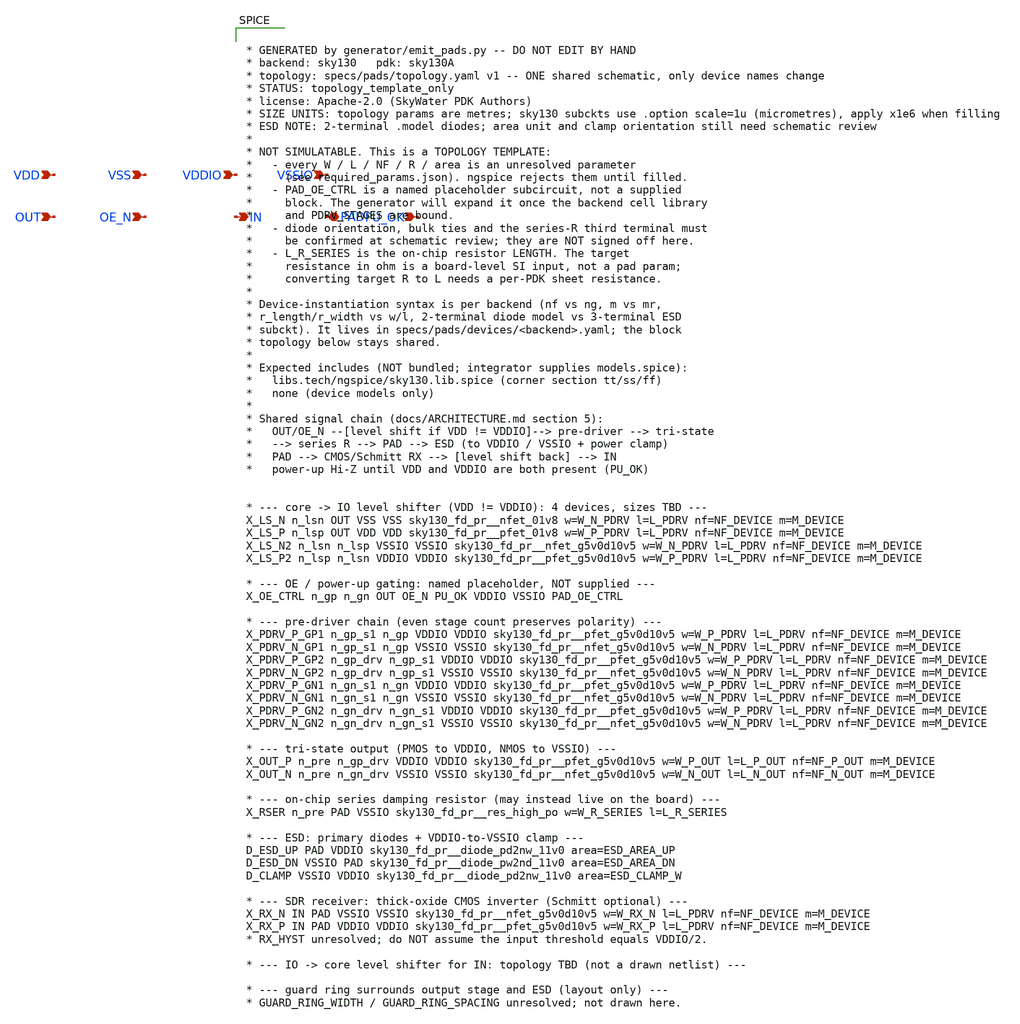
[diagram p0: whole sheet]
** sch_path: sch/pads/sky130/sdr_bidir_pad.sch
**.subckt sdr_bidir_pad OUT OE_N IN PAD PU_OK VDD VSS VDDIO VSSIO
*.ipin OUT
*.ipin OE_N
*.opin IN
*.iopin PAD
*.ipin PU_OK
*.ipin VDD
*.ipin VSS
*.ipin VDDIO
*.ipin VSSIO
**** begin user architecture code


* GENERATED by generator/emit_pads.py -- DO NOT EDIT BY HAND
* backend: sky130   pdk: sky130A
* topology: specs/pads/topology.yaml v1 -- ONE shared schematic, only device names change
* STATUS: topology_template_only
* license: Apache-2.0 (SkyWater PDK Authors)
* SIZE UNITS: topology params are metres; sky130 subckts use .option scale=1u (micrometres), apply
*+ x1e6 when filling
* ESD NOTE: 2-terminal .model diodes; area unit and clamp orientation still need schematic review
*
* NOT SIMULATABLE. This is a TOPOLOGY TEMPLATE:
*   - every W / L / NF / R / area is an unresolved parameter
*     (see required_params.json). ngspice rejects them until filled.
*   - PAD_OE_CTRL is a named placeholder subcircuit, not a supplied
*     block. The generator will expand it once the backend cell library
*     and PDRV_STAGES are bound.
*   - diode orientation, bulk ties and the series-R third terminal must
*     be confirmed at schematic review; they are NOT signed off here.
*   - L_R_SERIES is the on-chip resistor LENGTH. The target
*     resistance in ohm is a board-level SI input, not a pad param;
*     converting target R to L needs a per-PDK sheet resistance.
*
* Device-instantiation syntax is per backend (nf vs ng, m vs mr,
* r_length/r_width vs w/l, 2-terminal diode model vs 3-terminal ESD
* subckt). It lives in specs/pads/devices/<backend>.yaml; the block
* topology below stays shared.
*
* Expected includes (NOT bundled; integrator supplies models.spice):
*   libs.tech/ngspice/sky130.lib.spice (corner section tt/ss/ff)
*   none (device models only)
*
* Shared signal chain (docs/ARCHITECTURE.md section 5):
*   OUT/OE_N --[level shift if VDD != VDDIO]--> pre-driver --> tri-state
*   --> series R --> PAD --> ESD (to VDDIO / VSSIO + power clamp)
*   PAD --> CMOS/Schmitt RX --> [level shift back] --> IN
*   power-up Hi-Z until VDD and VDDIO are both present (PU_OK)


* --- core -> IO level shifter (VDD != VDDIO): 4 devices, sizes TBD ---
X_LS_N n_lsn OUT VSS VSS sky130_fd_pr__nfet_01v8 w=W_N_PDRV l=L_PDRV nf=NF_DEVICE m=M_DEVICE
X_LS_P n_lsp OUT VDD VDD sky130_fd_pr__pfet_01v8 w=W_P_PDRV l=L_PDRV nf=NF_DEVICE m=M_DEVICE
X_LS_N2 n_lsn n_lsp VSSIO VSSIO sky130_fd_pr__nfet_g5v0d10v5 w=W_N_PDRV l=L_PDRV nf=NF_DEVICE
+ m=M_DEVICE
X_LS_P2 n_lsp n_lsn VDDIO VDDIO sky130_fd_pr__pfet_g5v0d10v5 w=W_P_PDRV l=L_PDRV nf=NF_DEVICE
+ m=M_DEVICE

* --- OE / power-up gating: named placeholder, NOT supplied ---
X_OE_CTRL n_gp n_gn OUT OE_N PU_OK VDDIO VSSIO PAD_OE_CTRL

* --- pre-driver chain (even stage count preserves polarity) ---
X_PDRV_P_GP1 n_gp_s1 n_gp VDDIO VDDIO sky130_fd_pr__pfet_g5v0d10v5 w=W_P_PDRV l=L_PDRV nf=NF_DEVICE
+ m=M_DEVICE
X_PDRV_N_GP1 n_gp_s1 n_gp VSSIO VSSIO sky130_fd_pr__nfet_g5v0d10v5 w=W_N_PDRV l=L_PDRV nf=NF_DEVICE
+ m=M_DEVICE
X_PDRV_P_GP2 n_gp_drv n_gp_s1 VDDIO VDDIO sky130_fd_pr__pfet_g5v0d10v5 w=W_P_PDRV l=L_PDRV
+ nf=NF_DEVICE m=M_DEVICE
X_PDRV_N_GP2 n_gp_drv n_gp_s1 VSSIO VSSIO sky130_fd_pr__nfet_g5v0d10v5 w=W_N_PDRV l=L_PDRV
+ nf=NF_DEVICE m=M_DEVICE
X_PDRV_P_GN1 n_gn_s1 n_gn VDDIO VDDIO sky130_fd_pr__pfet_g5v0d10v5 w=W_P_PDRV l=L_PDRV nf=NF_DEVICE
+ m=M_DEVICE
X_PDRV_N_GN1 n_gn_s1 n_gn VSSIO VSSIO sky130_fd_pr__nfet_g5v0d10v5 w=W_N_PDRV l=L_PDRV nf=NF_DEVICE
+ m=M_DEVICE
X_PDRV_P_GN2 n_gn_drv n_gn_s1 VDDIO VDDIO sky130_fd_pr__pfet_g5v0d10v5 w=W_P_PDRV l=L_PDRV
+ nf=NF_DEVICE m=M_DEVICE
X_PDRV_N_GN2 n_gn_drv n_gn_s1 VSSIO VSSIO sky130_fd_pr__nfet_g5v0d10v5 w=W_N_PDRV l=L_PDRV
+ nf=NF_DEVICE m=M_DEVICE

* --- tri-state output (PMOS to VDDIO, NMOS to VSSIO) ---
X_OUT_P n_pre n_gp_drv VDDIO VDDIO sky130_fd_pr__pfet_g5v0d10v5 w=W_P_OUT l=L_P_OUT nf=NF_P_OUT
+ m=M_DEVICE
X_OUT_N n_pre n_gn_drv VSSIO VSSIO sky130_fd_pr__nfet_g5v0d10v5 w=W_N_OUT l=L_N_OUT nf=NF_N_OUT
+ m=M_DEVICE

* --- on-chip series damping resistor (may instead live on the board) ---
X_RSER n_pre PAD VSSIO sky130_fd_pr__res_high_po w=W_R_SERIES l=L_R_SERIES

* --- ESD: primary diodes + VDDIO-to-VSSIO clamp ---
D_ESD_UP PAD VDDIO sky130_fd_pr__diode_pd2nw_11v0 area=ESD_AREA_UP
D_ESD_DN VSSIO PAD sky130_fd_pr__diode_pw2nd_11v0 area=ESD_AREA_DN
D_CLAMP VSSIO VDDIO sky130_fd_pr__diode_pd2nw_11v0 area=ESD_CLAMP_W

* --- SDR receiver: thick-oxide CMOS inverter (Schmitt optional) ---
X_RX_N IN PAD VSSIO VSSIO sky130_fd_pr__nfet_g5v0d10v5 w=W_RX_N l=L_PDRV nf=NF_DEVICE m=M_DEVICE
X_RX_P IN PAD VDDIO VDDIO sky130_fd_pr__pfet_g5v0d10v5 w=W_RX_P l=L_PDRV nf=NF_DEVICE m=M_DEVICE
* RX_HYST unresolved; do NOT assume the input threshold equals VDDIO/2.

* --- IO -> core level shifter for IN: topology TBD (not a drawn netlist) ---

* --- guard ring surrounds output stage and ESD (layout only) ---
* GUARD_RING_WIDTH / GUARD_RING_SPACING unresolved; not drawn here.


**** end user architecture code
**.ends
.end
